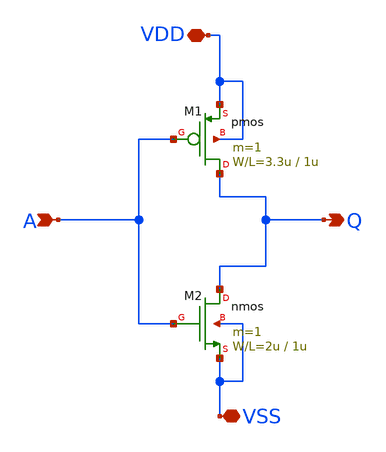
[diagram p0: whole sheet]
** sch_path: member_project/YutakaKOTANI/inv_yutaka.sch
**.subckt inv_yutaka VDD VSS A Q
*.iopin VDD
*.iopin VSS
*.ipin A
*.opin Q
M1 Q A VDD VDD pmos L=1u W=3.3u m=1
M2 Q A VSS VSS nmos L=1u W=2u m=1
**.ends
.end
